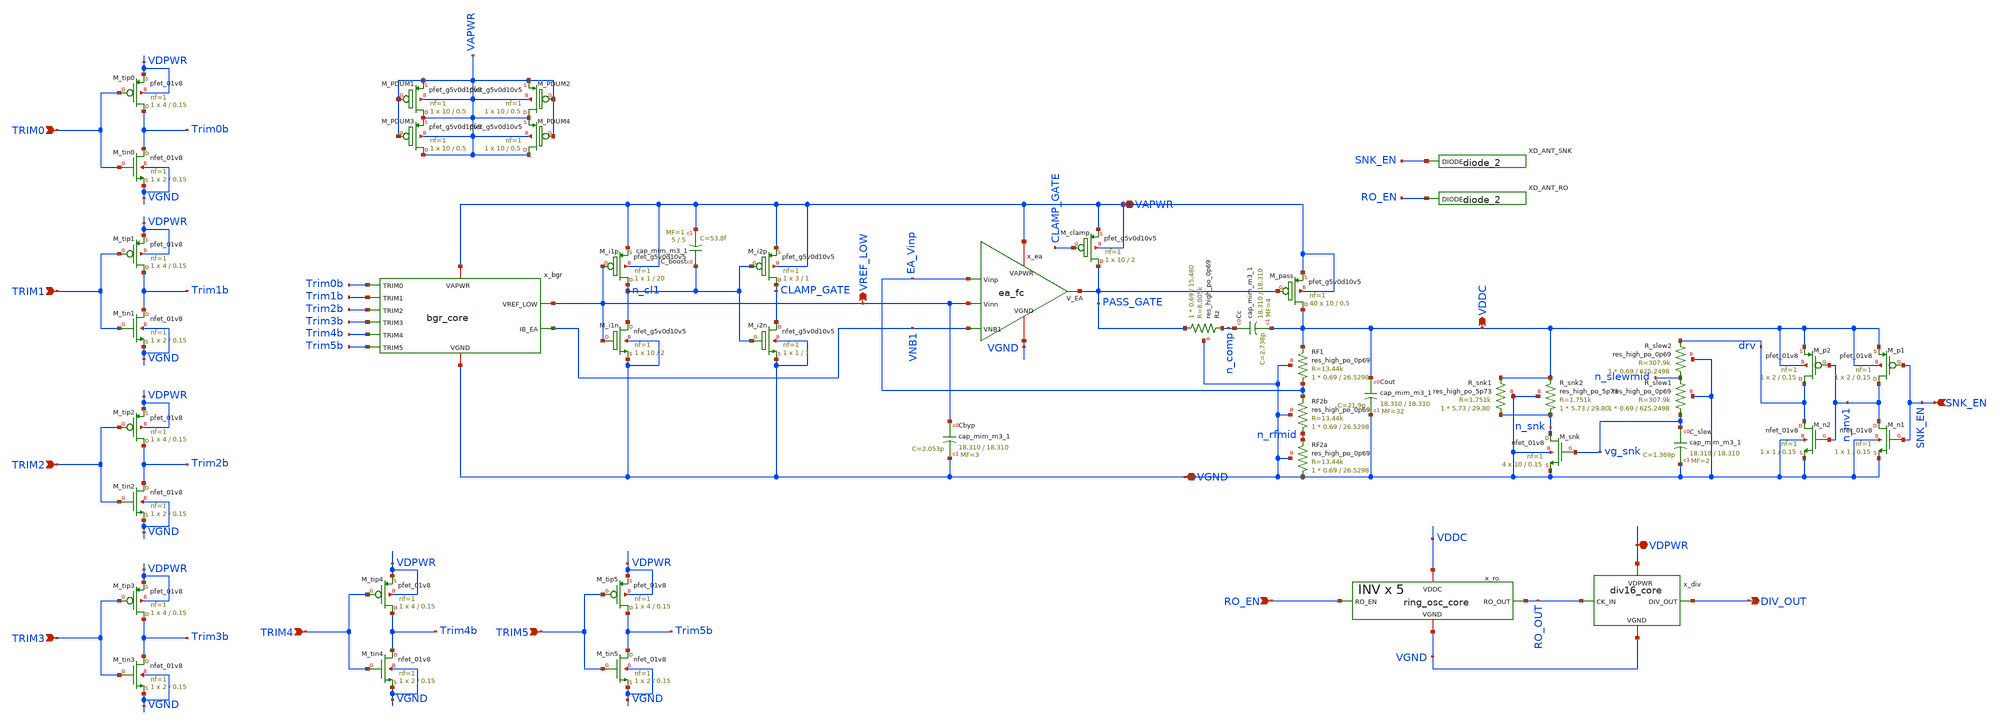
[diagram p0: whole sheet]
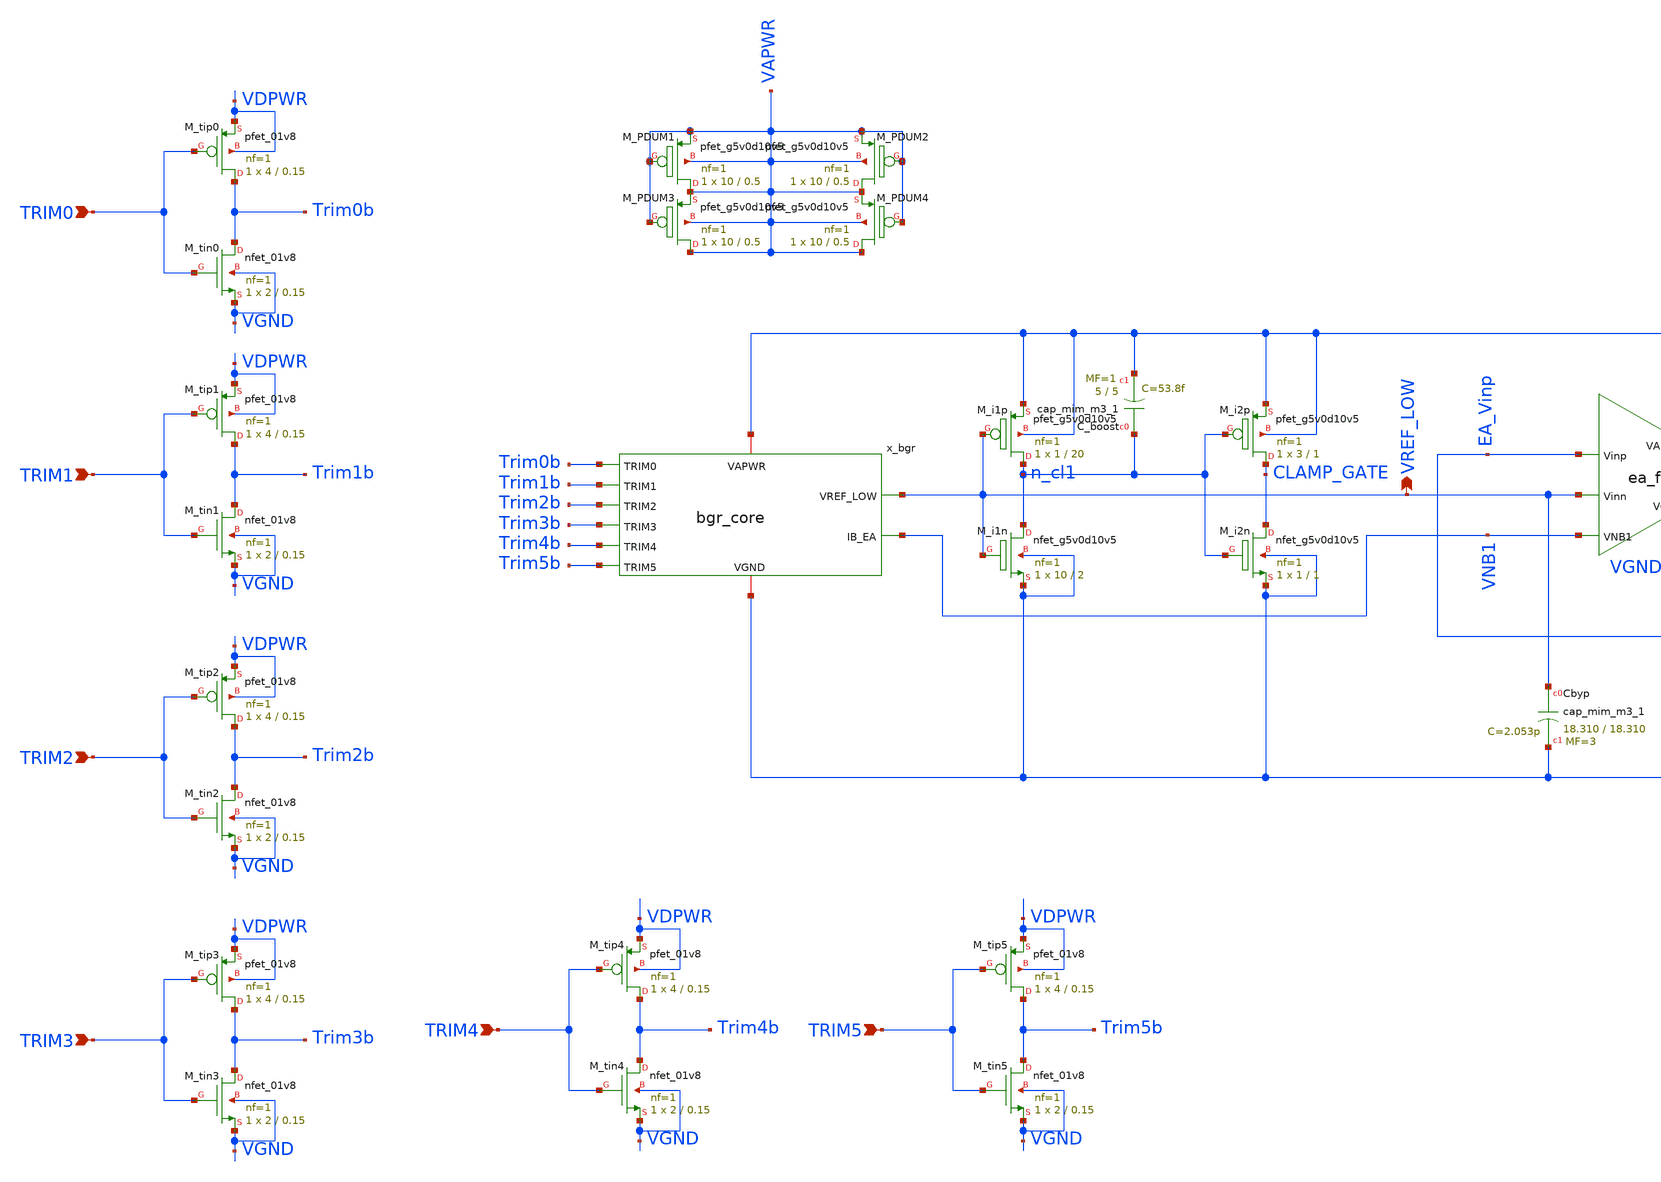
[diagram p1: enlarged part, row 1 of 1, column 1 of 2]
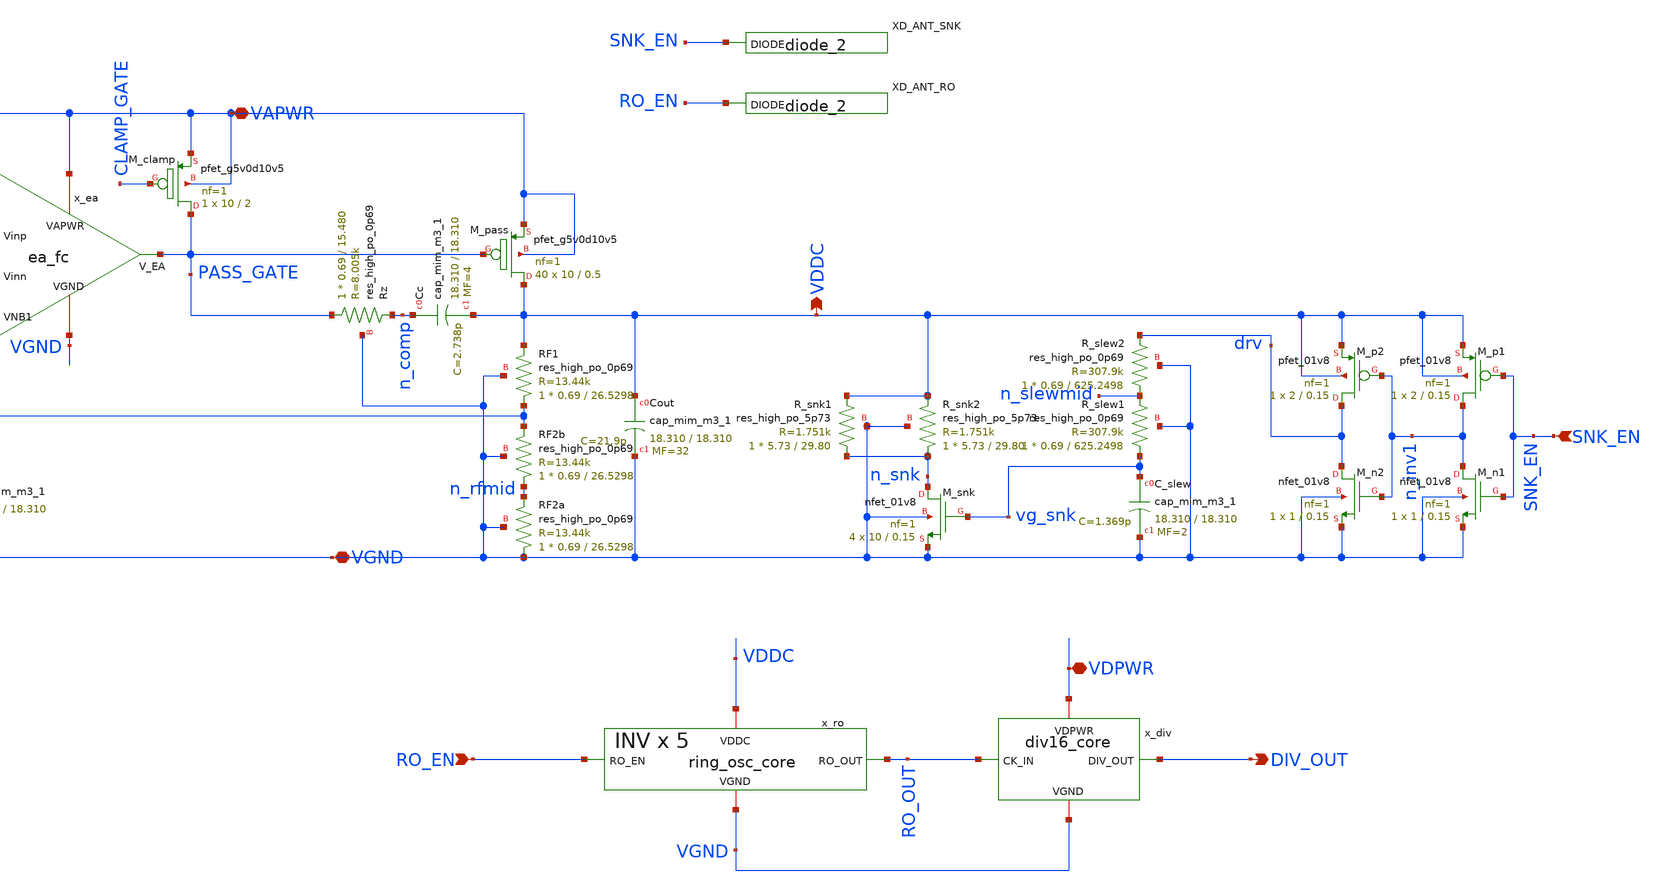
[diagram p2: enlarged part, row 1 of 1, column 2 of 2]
** sch_path: designs/bgr_ldo/ldo/ldo_top.sch
**.subckt ldo_top TRIM0 TRIM1 TRIM2 TRIM3 SNK_EN VDPWR VGND VAPWR RO_EN DIV_OUT VREF_LOW VDDC TRIM4
*+ TRIM5
*.ipin TRIM0
*.ipin TRIM1
*.ipin TRIM2
*.ipin TRIM3
*.ipin SNK_EN
*.iopin VDPWR
*.iopin VGND
*.iopin VAPWR
*.ipin RO_EN
*.opin DIV_OUT
*.opin VREF_LOW
*.opin VDDC
*.ipin TRIM4
*.ipin TRIM5
XM_tip0 Trim0b TRIM0 VDPWR VDPWR sky130_fd_pr__pfet_01v8 L=0.15 W=4 nf=1 ad='int((1 + 1)/2) * 4 / 1 * 0.29'
+ as='int((1 + 2)/2) * 4 / 1 * 0.29' pd='2*int((1 + 1)/2) * (4 / 1 + 0.29)' ps='2*int((1 + 2)/2) * (4 / 1 + 0.29)'
+ nrd='0.29 / 4 ' nrs='0.29 / 4 ' sa=0 sb=0 sd=0 mult=1 m=1
XM_tin0 Trim0b TRIM0 VGND VGND sky130_fd_pr__nfet_01v8 L=0.15 W=2 nf=1 ad='int((1 + 1)/2) * 2 / 1 * 0.29'
+ as='int((1 + 2)/2) * 2 / 1 * 0.29' pd='2*int((1 + 1)/2) * (2 / 1 + 0.29)' ps='2*int((1 + 2)/2) * (2 / 1 + 0.29)'
+ nrd='0.29 / 2 ' nrs='0.29 / 2 ' sa=0 sb=0 sd=0 mult=1 m=1
XM_tip1 Trim1b TRIM1 VDPWR VDPWR sky130_fd_pr__pfet_01v8 L=0.15 W=4 nf=1 ad='int((1 + 1)/2) * 4 / 1 * 0.29'
+ as='int((1 + 2)/2) * 4 / 1 * 0.29' pd='2*int((1 + 1)/2) * (4 / 1 + 0.29)' ps='2*int((1 + 2)/2) * (4 / 1 + 0.29)'
+ nrd='0.29 / 4 ' nrs='0.29 / 4 ' sa=0 sb=0 sd=0 mult=1 m=1
XM_tin1 Trim1b TRIM1 VGND VGND sky130_fd_pr__nfet_01v8 L=0.15 W=2 nf=1 ad='int((1 + 1)/2) * 2 / 1 * 0.29'
+ as='int((1 + 2)/2) * 2 / 1 * 0.29' pd='2*int((1 + 1)/2) * (2 / 1 + 0.29)' ps='2*int((1 + 2)/2) * (2 / 1 + 0.29)'
+ nrd='0.29 / 2 ' nrs='0.29 / 2 ' sa=0 sb=0 sd=0 mult=1 m=1
XM_tip2 Trim2b TRIM2 VDPWR VDPWR sky130_fd_pr__pfet_01v8 L=0.15 W=4 nf=1 ad='int((1 + 1)/2) * 4 / 1 * 0.29'
+ as='int((1 + 2)/2) * 4 / 1 * 0.29' pd='2*int((1 + 1)/2) * (4 / 1 + 0.29)' ps='2*int((1 + 2)/2) * (4 / 1 + 0.29)'
+ nrd='0.29 / 4 ' nrs='0.29 / 4 ' sa=0 sb=0 sd=0 mult=1 m=1
XM_tin2 Trim2b TRIM2 VGND VGND sky130_fd_pr__nfet_01v8 L=0.15 W=2 nf=1 ad='int((1 + 1)/2) * 2 / 1 * 0.29'
+ as='int((1 + 2)/2) * 2 / 1 * 0.29' pd='2*int((1 + 1)/2) * (2 / 1 + 0.29)' ps='2*int((1 + 2)/2) * (2 / 1 + 0.29)'
+ nrd='0.29 / 2 ' nrs='0.29 / 2 ' sa=0 sb=0 sd=0 mult=1 m=1
XM_tip3 Trim3b TRIM3 VDPWR VDPWR sky130_fd_pr__pfet_01v8 L=0.15 W=4 nf=1 ad='int((1 + 1)/2) * 4 / 1 * 0.29'
+ as='int((1 + 2)/2) * 4 / 1 * 0.29' pd='2*int((1 + 1)/2) * (4 / 1 + 0.29)' ps='2*int((1 + 2)/2) * (4 / 1 + 0.29)'
+ nrd='0.29 / 4 ' nrs='0.29 / 4 ' sa=0 sb=0 sd=0 mult=1 m=1
XM_tin3 Trim3b TRIM3 VGND VGND sky130_fd_pr__nfet_01v8 L=0.15 W=2 nf=1 ad='int((1 + 1)/2) * 2 / 1 * 0.29'
+ as='int((1 + 2)/2) * 2 / 1 * 0.29' pd='2*int((1 + 1)/2) * (2 / 1 + 0.29)' ps='2*int((1 + 2)/2) * (2 / 1 + 0.29)'
+ nrd='0.29 / 2 ' nrs='0.29 / 2 ' sa=0 sb=0 sd=0 mult=1 m=1
x_ro VDDC RO_EN VGND RO_OUT ring_osc_core
XM_pass VDDC PASS_GATE VAPWR VAPWR sky130_fd_pr__pfet_g5v0d10v5 L=0.5 W=10 nf=1 ad='int((1 + 1)/2) * 10 / 1 * 0.29'
+ as='int((1 + 2)/2) * 10 / 1 * 0.29' pd='2*int((1 + 1)/2) * (10 / 1 + 0.29)' ps='2*int((1 + 2)/2) * (10 / 1 + 0.29)'
+ nrd='0.29 / 10 ' nrs='0.29 / 10 ' sa=0 sb=0 sd=0 mult=40 m=40
x_ea VAPWR PASS_GATE EA_Vinp VREF_LOW VNB1 VGND ea_fc
XRF1 EA_Vinp VDDC VGND sky130_fd_pr__res_high_po_0p69 L=26.5298 mult=1 m=1
XRF2a VGND n_rfmid VGND sky130_fd_pr__res_high_po_0p69 L=26.5298 mult=1 m=1
XRz PASS_GATE n_comp VGND sky130_fd_pr__res_high_po_0p69 L=15.480 mult=1 m=1
XCout VDDC VGND sky130_fd_pr__cap_mim_m3_1 W=18.310 L=18.310 MF=32 m=32
XCc n_comp VDDC sky130_fd_pr__cap_mim_m3_1 W=18.310 L=18.310 MF=4 m=4
x_bgr VAPWR VREF_LOW VNB1 Trim0b Trim1b Trim2b Trim3b Trim4b Trim5b VGND bgr_core
XCbyp VREF_LOW VGND sky130_fd_pr__cap_mim_m3_1 W=18.310 L=18.310 MF=3 m=3
XR_slew2 n_slewmid drv VGND sky130_fd_pr__res_high_po_0p69 L=625.2498 mult=1 m=1
XC_slew vg_snk VGND sky130_fd_pr__cap_mim_m3_1 W=18.310 L=18.310 MF=2 m=2
XM_p1 n_inv1 SNK_EN VDDC VDDC sky130_fd_pr__pfet_01v8 L=0.15 W=2 nf=1 ad='int((1 + 1)/2) * 2 / 1 * 0.29'
+ as='int((1 + 2)/2) * 2 / 1 * 0.29' pd='2*int((1 + 1)/2) * (2 / 1 + 0.29)' ps='2*int((1 + 2)/2) * (2 / 1 + 0.29)'
+ nrd='0.29 / 2 ' nrs='0.29 / 2 ' sa=0 sb=0 sd=0 mult=1 m=1
XM_p2 drv n_inv1 VDDC VDDC sky130_fd_pr__pfet_01v8 L=0.15 W=2 nf=1 ad='int((1 + 1)/2) * 2 / 1 * 0.29'
+ as='int((1 + 2)/2) * 2 / 1 * 0.29' pd='2*int((1 + 1)/2) * (2 / 1 + 0.29)' ps='2*int((1 + 2)/2) * (2 / 1 + 0.29)'
+ nrd='0.29 / 2 ' nrs='0.29 / 2 ' sa=0 sb=0 sd=0 mult=1 m=1
XR_snk2 n_snk VDDC VGND sky130_fd_pr__res_high_po_5p73 L=29.80 mult=1 m=1
x_div VDPWR VGND DIV_OUT RO_OUT div16_core
XM_i1p n_cl1 VREF_LOW VAPWR VAPWR sky130_fd_pr__pfet_g5v0d10v5 L=20 W=1 nf=1 ad='int((1 + 1)/2) * 1 / 1 * 0.29'
+ as='int((1 + 2)/2) * 1 / 1 * 0.29' pd='2*int((1 + 1)/2) * (1 / 1 + 0.29)' ps='2*int((1 + 2)/2) * (1 / 1 + 0.29)'
+ nrd='0.29 / 1 ' nrs='0.29 / 1 ' sa=0 sb=0 sd=0 mult=1 m=1
XM_snk n_snk vg_snk VGND VGND sky130_fd_pr__nfet_01v8 L=0.15 W=10 nf=1 ad='int((1 + 1)/2) * 10 / 1 * 0.29'
+ as='int((1 + 2)/2) * 10 / 1 * 0.29' pd='2*int((1 + 1)/2) * (10 / 1 + 0.29)' ps='2*int((1 + 2)/2) * (10 / 1 + 0.29)'
+ nrd='0.29 / 10 ' nrs='0.29 / 10 ' sa=0 sb=0 sd=0 mult=4 m=4
XM_n2 drv n_inv1 VGND VGND sky130_fd_pr__nfet_01v8 L=0.15 W=1 nf=1 ad='int((1 + 1)/2) * 1 / 1 * 0.29'
+ as='int((1 + 2)/2) * 1 / 1 * 0.29' pd='2*int((1 + 1)/2) * (1 / 1 + 0.29)' ps='2*int((1 + 2)/2) * (1 / 1 + 0.29)'
+ nrd='0.29 / 1 ' nrs='0.29 / 1 ' sa=0 sb=0 sd=0 mult=1 m=1
XM_n1 n_inv1 SNK_EN VGND VGND sky130_fd_pr__nfet_01v8 L=0.15 W=1 nf=1 ad='int((1 + 1)/2) * 1 / 1 * 0.29'
+ as='int((1 + 2)/2) * 1 / 1 * 0.29' pd='2*int((1 + 1)/2) * (1 / 1 + 0.29)' ps='2*int((1 + 2)/2) * (1 / 1 + 0.29)'
+ nrd='0.29 / 1 ' nrs='0.29 / 1 ' sa=0 sb=0 sd=0 mult=1 m=1
XM_i1n n_cl1 VREF_LOW VGND VGND sky130_fd_pr__nfet_g5v0d10v5 L=2 W=10 nf=1 ad='int((1 + 1)/2) * 10 / 1 * 0.29'
+ as='int((1 + 2)/2) * 10 / 1 * 0.29' pd='2*int((1 + 1)/2) * (10 / 1 + 0.29)' ps='2*int((1 + 2)/2) * (10 / 1 + 0.29)'
+ nrd='0.29 / 10 ' nrs='0.29 / 10 ' sa=0 sb=0 sd=0 mult=1 m=1
XM_i2n CLAMP_GATE n_cl1 VGND VGND sky130_fd_pr__nfet_g5v0d10v5 L=1 W=1 nf=1 ad='int((1 + 1)/2) * 1 / 1 * 0.29'
+ as='int((1 + 2)/2) * 1 / 1 * 0.29' pd='2*int((1 + 1)/2) * (1 / 1 + 0.29)' ps='2*int((1 + 2)/2) * (1 / 1 + 0.29)'
+ nrd='0.29 / 1 ' nrs='0.29 / 1 ' sa=0 sb=0 sd=0 mult=1 m=1
XM_i2p CLAMP_GATE n_cl1 VAPWR VAPWR sky130_fd_pr__pfet_g5v0d10v5 L=1 W=3 nf=1 ad='int((1 + 1)/2) * 3 / 1 * 0.29'
+ as='int((1 + 2)/2) * 3 / 1 * 0.29' pd='2*int((1 + 1)/2) * (3 / 1 + 0.29)' ps='2*int((1 + 2)/2) * (3 / 1 + 0.29)'
+ nrd='0.29 / 3 ' nrs='0.29 / 3 ' sa=0 sb=0 sd=0 mult=1 m=1
XM_clamp PASS_GATE CLAMP_GATE VAPWR VAPWR sky130_fd_pr__pfet_g5v0d10v5 L=2 W=10 nf=1 ad='int((1 + 1)/2) * 10 / 1 * 0.29'
+ as='int((1 + 2)/2) * 10 / 1 * 0.29' pd='2*int((1 + 1)/2) * (10 / 1 + 0.29)' ps='2*int((1 + 2)/2) * (10 / 1 + 0.29)'
+ nrd='0.29 / 10 ' nrs='0.29 / 10 ' sa=0 sb=0 sd=0 mult=1 m=1
XC_boost n_cl1 VAPWR sky130_fd_pr__cap_mim_m3_1 W=5 L=5 MF=1 m=1
XR_slew1 vg_snk n_slewmid VGND sky130_fd_pr__res_high_po_0p69 L=625.2498 mult=1 m=1
XRF2b n_rfmid EA_Vinp VGND sky130_fd_pr__res_high_po_0p69 L=26.5298 mult=1 m=1
XR_snk1 n_snk VDDC VGND sky130_fd_pr__res_high_po_5p73 L=29.80 mult=1 m=1
XM_PDUM1 VAPWR VAPWR VAPWR VAPWR sky130_fd_pr__pfet_g5v0d10v5 L=0.5 W=10 nf=1 ad='int((1 + 1)/2) * 10 / 1 * 0.29'
+ as='int((1 + 2)/2) * 10 / 1 * 0.29' pd='2*int((1 + 1)/2) * (10 / 1 + 0.29)' ps='2*int((1 + 2)/2) * (10 / 1 + 0.29)'
+ nrd='0.29 / 10 ' nrs='0.29 / 10 ' sa=0 sb=0 sd=0 mult=1 m=1
XM_PDUM2 VAPWR VAPWR VAPWR VAPWR sky130_fd_pr__pfet_g5v0d10v5 L=0.5 W=10 nf=1 ad='int((1 + 1)/2) * 10 / 1 * 0.29'
+ as='int((1 + 2)/2) * 10 / 1 * 0.29' pd='2*int((1 + 1)/2) * (10 / 1 + 0.29)' ps='2*int((1 + 2)/2) * (10 / 1 + 0.29)'
+ nrd='0.29 / 10 ' nrs='0.29 / 10 ' sa=0 sb=0 sd=0 mult=1 m=1
XM_PDUM3 VAPWR VAPWR VAPWR VAPWR sky130_fd_pr__pfet_g5v0d10v5 L=0.5 W=10 nf=1 ad='int((1 + 1)/2) * 10 / 1 * 0.29'
+ as='int((1 + 2)/2) * 10 / 1 * 0.29' pd='2*int((1 + 1)/2) * (10 / 1 + 0.29)' ps='2*int((1 + 2)/2) * (10 / 1 + 0.29)'
+ nrd='0.29 / 10 ' nrs='0.29 / 10 ' sa=0 sb=0 sd=0 mult=1 m=1
XM_PDUM4 VAPWR VAPWR VAPWR VAPWR sky130_fd_pr__pfet_g5v0d10v5 L=0.5 W=10 nf=1 ad='int((1 + 1)/2) * 10 / 1 * 0.29'
+ as='int((1 + 2)/2) * 10 / 1 * 0.29' pd='2*int((1 + 1)/2) * (10 / 1 + 0.29)' ps='2*int((1 + 2)/2) * (10 / 1 + 0.29)'
+ nrd='0.29 / 10 ' nrs='0.29 / 10 ' sa=0 sb=0 sd=0 mult=1 m=1
XD_ANT_SNK SNK_EN VGND VGND VDPWR VDPWR sky130_fd_sc_hd__diode_2
XD_ANT_RO RO_EN VGND VGND VDPWR VDPWR sky130_fd_sc_hd__diode_2
XM_tip4 Trim4b TRIM4 VDPWR VDPWR sky130_fd_pr__pfet_01v8 L=0.15 W=4 nf=1 ad='int((1 + 1)/2) * 4 / 1 * 0.29'
+ as='int((1 + 2)/2) * 4 / 1 * 0.29' pd='2*int((1 + 1)/2) * (4 / 1 + 0.29)' ps='2*int((1 + 2)/2) * (4 / 1 + 0.29)'
+ nrd='0.29 / 4 ' nrs='0.29 / 4 ' sa=0 sb=0 sd=0 mult=1 m=1
XM_tin4 Trim4b TRIM4 VGND VGND sky130_fd_pr__nfet_01v8 L=0.15 W=2 nf=1 ad='int((1 + 1)/2) * 2 / 1 * 0.29'
+ as='int((1 + 2)/2) * 2 / 1 * 0.29' pd='2*int((1 + 1)/2) * (2 / 1 + 0.29)' ps='2*int((1 + 2)/2) * (2 / 1 + 0.29)'
+ nrd='0.29 / 2 ' nrs='0.29 / 2 ' sa=0 sb=0 sd=0 mult=1 m=1
XM_tip5 Trim5b TRIM5 VDPWR VDPWR sky130_fd_pr__pfet_01v8 L=0.15 W=4 nf=1 ad='int((1 + 1)/2) * 4 / 1 * 0.29'
+ as='int((1 + 2)/2) * 4 / 1 * 0.29' pd='2*int((1 + 1)/2) * (4 / 1 + 0.29)' ps='2*int((1 + 2)/2) * (4 / 1 + 0.29)'
+ nrd='0.29 / 4 ' nrs='0.29 / 4 ' sa=0 sb=0 sd=0 mult=1 m=1
XM_tin5 Trim5b TRIM5 VGND VGND sky130_fd_pr__nfet_01v8 L=0.15 W=2 nf=1 ad='int((1 + 1)/2) * 2 / 1 * 0.29'
+ as='int((1 + 2)/2) * 2 / 1 * 0.29' pd='2*int((1 + 1)/2) * (2 / 1 + 0.29)' ps='2*int((1 + 2)/2) * (2 / 1 + 0.29)'
+ nrd='0.29 / 2 ' nrs='0.29 / 2 ' sa=0 sb=0 sd=0 mult=1 m=1
**.ends
.end
